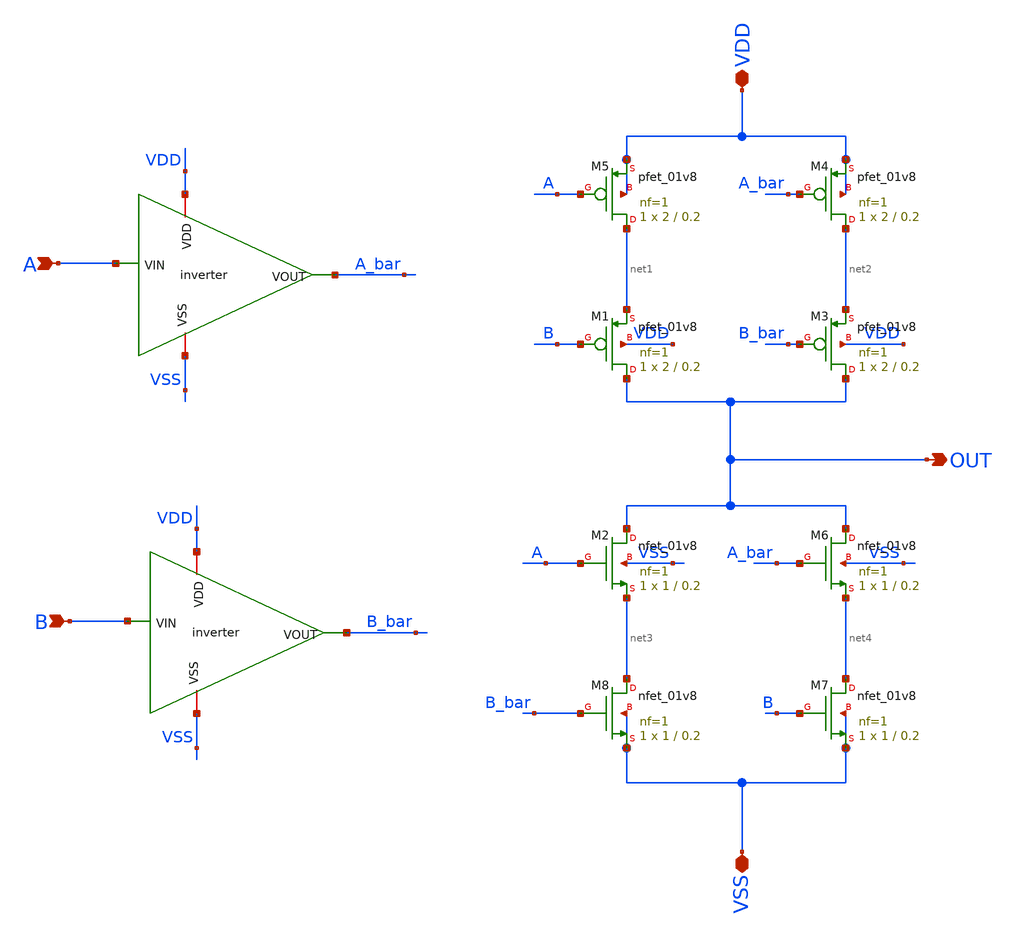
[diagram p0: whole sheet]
** sch_path: Xschem/PLL_TOP_Schematics/XNOR.sch
* Xschem/PLL_TOP_Schematics/inverter.sch:
* Copyright 2022 GlobalFoundries PDK Authors
* Licensed under the Apache License, Version 2.0 (the "License");
**.subckt XNOR VDD VSS A B OUT
*.iopin VDD
*.iopin VSS
*.ipin A
*.ipin B
*.opin OUT
x1 VDD A A_bar VSS inverter
x2 VDD B B_bar VSS inverter
XM5 net1 A VDD VDD sky130_fd_pr__pfet_01v8 L=0.2 W=2 nf=1 ad='int((nf+1)/2) * W/nf * 0.29' as='int((nf+2)/2) * W/nf * 0.29'
+ pd='2*int((nf+1)/2) * (W/nf + 0.29)' ps='2*int((nf+2)/2) * (W/nf + 0.29)' nrd='0.29 / W' nrs='0.29 / W'
+ sa=0 sb=0 sd=0 mult=1 m=1
XM2 OUT A net3 VSS sky130_fd_pr__nfet_01v8 L=0.2 W=1 nf=1 ad='int((nf+1)/2) * W/nf * 0.29' as='int((nf+2)/2) * W/nf * 0.29'
+ pd='2*int((nf+1)/2) * (W/nf + 0.29)' ps='2*int((nf+2)/2) * (W/nf + 0.29)' nrd='0.29 / W' nrs='0.29 / W'
+ sa=0 sb=0 sd=0 mult=1 m=1
XM1 OUT B net1 VDD sky130_fd_pr__pfet_01v8 L=0.2 W=2 nf=1 ad='int((nf+1)/2) * W/nf * 0.29' as='int((nf+2)/2) * W/nf * 0.29'
+ pd='2*int((nf+1)/2) * (W/nf + 0.29)' ps='2*int((nf+2)/2) * (W/nf + 0.29)' nrd='0.29 / W' nrs='0.29 / W'
+ sa=0 sb=0 sd=0 mult=1 m=1
XM3 OUT B_bar net2 VDD sky130_fd_pr__pfet_01v8 L=0.2 W=2 nf=1 ad='int((nf+1)/2) * W/nf * 0.29' as='int((nf+2)/2) * W/nf * 0.29'
+ pd='2*int((nf+1)/2) * (W/nf + 0.29)' ps='2*int((nf+2)/2) * (W/nf + 0.29)' nrd='0.29 / W' nrs='0.29 / W'
+ sa=0 sb=0 sd=0 mult=1 m=1
XM4 net2 A_bar VDD VDD sky130_fd_pr__pfet_01v8 L=0.2 W=2 nf=1 ad='int((nf+1)/2) * W/nf * 0.29' as='int((nf+2)/2) * W/nf * 0.29'
+ pd='2*int((nf+1)/2) * (W/nf + 0.29)' ps='2*int((nf+2)/2) * (W/nf + 0.29)' nrd='0.29 / W' nrs='0.29 / W'
+ sa=0 sb=0 sd=0 mult=1 m=1
XM6 OUT A_bar net4 VSS sky130_fd_pr__nfet_01v8 L=0.2 W=1 nf=1 ad='int((nf+1)/2) * W/nf * 0.29' as='int((nf+2)/2) * W/nf * 0.29'
+ pd='2*int((nf+1)/2) * (W/nf + 0.29)' ps='2*int((nf+2)/2) * (W/nf + 0.29)' nrd='0.29 / W' nrs='0.29 / W'
+ sa=0 sb=0 sd=0 mult=1 m=1
XM7 net4 B VSS VSS sky130_fd_pr__nfet_01v8 L=0.2 W=1 nf=1 ad='int((nf+1)/2) * W/nf * 0.29' as='int((nf+2)/2) * W/nf * 0.29'
+ pd='2*int((nf+1)/2) * (W/nf + 0.29)' ps='2*int((nf+2)/2) * (W/nf + 0.29)' nrd='0.29 / W' nrs='0.29 / W'
+ sa=0 sb=0 sd=0 mult=1 m=1
XM8 net3 B_bar VSS VSS sky130_fd_pr__nfet_01v8 L=0.2 W=1 nf=1 ad='int((nf+1)/2) * W/nf * 0.29' as='int((nf+2)/2) * W/nf * 0.29'
+ pd='2*int((nf+1)/2) * (W/nf + 0.29)' ps='2*int((nf+2)/2) * (W/nf + 0.29)' nrd='0.29 / W' nrs='0.29 / W'
+ sa=0 sb=0 sd=0 mult=1 m=1
**.ends

* expanding   symbol:  inverter.sym # of pins=4
** sym_path: Xschem/PLL_TOP_Schematics/inverter.sym
** sch_path: Xschem/PLL_TOP_Schematics/inverter.sch
.subckt inverter VDD VIN VOUT VSS
*.iopin VDD
*.ipin VIN
*.opin VOUT
*.iopin VSS
XM5 VOUT VIN VDD VDD sky130_fd_pr__pfet_01v8 L=0.2 W=5 nf=1 ad='int((nf+1)/2) * W/nf * 0.29' as='int((nf+2)/2) * W/nf * 0.29'
+ pd='2*int((nf+1)/2) * (W/nf + 0.29)' ps='2*int((nf+2)/2) * (W/nf + 0.29)' nrd='0.29 / W' nrs='0.29 / W'
+ sa=0 sb=0 sd=0 mult=1 m=1
XM1 VOUT VIN VSS VSS sky130_fd_pr__nfet_01v8 L=0.2 W=2.5 nf=1 ad='int((nf+1)/2) * W/nf * 0.29' as='int((nf+2)/2) * W/nf * 0.29'
+ pd='2*int((nf+1)/2) * (W/nf + 0.29)' ps='2*int((nf+2)/2) * (W/nf + 0.29)' nrd='0.29 / W' nrs='0.29 / W'
+ sa=0 sb=0 sd=0 mult=1 m=1
.ends

.end
